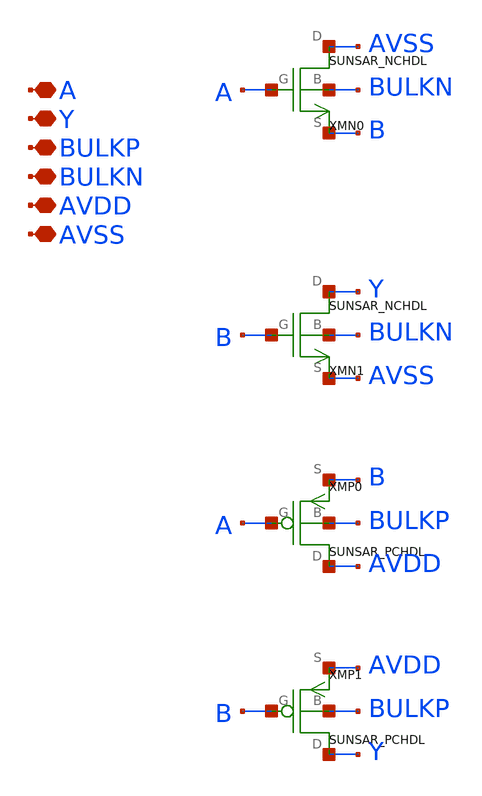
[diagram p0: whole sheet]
** sch_path: design/SUN_SAR9B_SKY130NM/SUNSAR_BFX1_CV.sch
**.subckt SUNSAR_BFX1_CV A Y BULKP BULKN AVDD AVSS
*.iopin A
*.iopin Y
*.iopin BULKP
*.iopin BULKN
*.iopin AVDD
*.iopin AVSS
XMN0 AVSS A B BULKN SUNSAR_NCHDL
XMN1 Y B AVSS BULKN SUNSAR_NCHDL
XMP0 AVDD A B BULKP SUNSAR_PCHDL
XMP1 Y B AVDD BULKP SUNSAR_PCHDL
**.ends
.end
